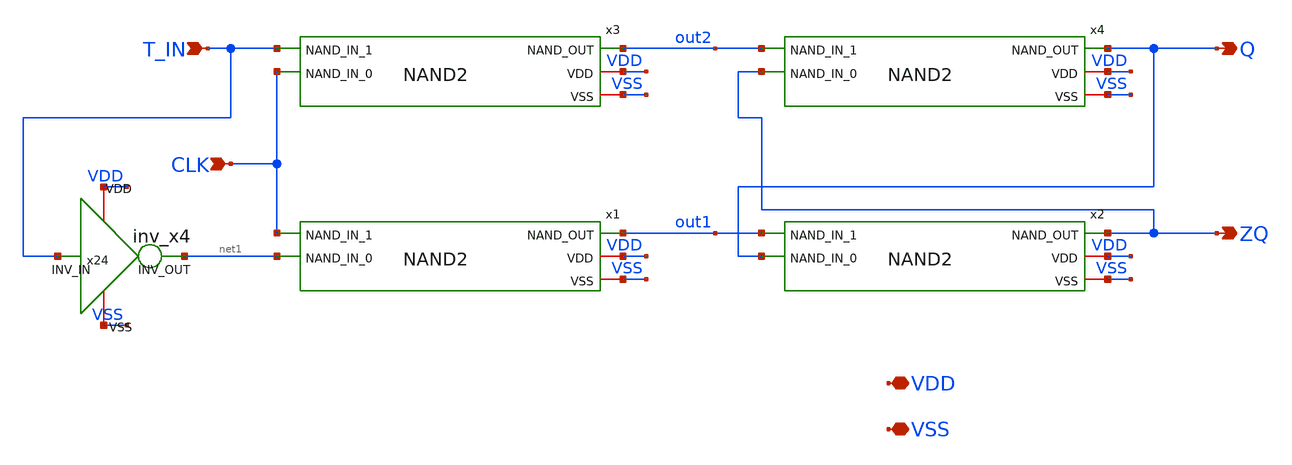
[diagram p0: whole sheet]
** sch_path: xschem/T_FLIP_FLOP.sch
**.subckt T_FLIP_FLOP VDD VSS CLK ZQ Q T_IN
*.iopin VDD
*.iopin VSS
*.ipin CLK
*.opin ZQ
*.opin Q
*.ipin T_IN
x2 ZQ VDD out1 VSS Q NAND2
x4 Q VDD out2 VSS ZQ NAND2
x1 out1 VDD CLK VSS net1 NAND2
x3 out2 VDD T_IN VSS CLK NAND2
x24 VDD VSS net1 T_IN inv_x4
**.ends

* expanding   symbol:  NAND2.sym # of pins=5
** sym_path: xschem/NAND2.sym
** sch_path: xschem/NAND2.sch
.subckt NAND2 NAND_OUT VDD NAND_IN_1 VSS NAND_IN_0
*.ipin NAND_IN_0
*.opin NAND_OUT
*.iopin VDD
*.iopin VSS
*.ipin NAND_IN_1
XM0 net1 NAND_IN_0 VSS VSS sky130_fd_pr__nfet_01v8 L=0.15 W=1 nf=1 ad='int((nf+1)/2) * W/nf * 0.29' as='int((nf+2)/2) * W/nf * 0.29'
+ pd='2*int((nf+1)/2) * (W/nf + 0.29)' ps='2*int((nf+2)/2) * (W/nf + 0.29)' nrd='0.29 / W' nrs='0.29 / W'
+ sa=0 sb=0 sd=0 mult=1 m=1
XM1 NAND_OUT NAND_IN_1 net1 VSS sky130_fd_pr__nfet_01v8 L=0.15 W=1 nf=1 ad='int((nf+1)/2) * W/nf * 0.29'
+ as='int((nf+2)/2) * W/nf * 0.29' pd='2*int((nf+1)/2) * (W/nf + 0.29)' ps='2*int((nf+2)/2) * (W/nf + 0.29)'
+ nrd='0.29 / W' nrs='0.29 / W' sa=0 sb=0 sd=0 mult=1 m=1
XM12 NAND_OUT NAND_IN_0 VDD VDD sky130_fd_pr__pfet_01v8 L=0.15 W=1 nf=1 ad='int((nf+1)/2) * W/nf * 0.29'
+ as='int((nf+2)/2) * W/nf * 0.29' pd='2*int((nf+1)/2) * (W/nf + 0.29)' ps='2*int((nf+2)/2) * (W/nf + 0.29)'
+ nrd='0.29 / W' nrs='0.29 / W' sa=0 sb=0 sd=0 mult=1 m=1
XM13 NAND_OUT NAND_IN_1 VDD VDD sky130_fd_pr__pfet_01v8 L=0.15 W=1 nf=1 ad='int((nf+1)/2) * W/nf * 0.29'
+ as='int((nf+2)/2) * W/nf * 0.29' pd='2*int((nf+1)/2) * (W/nf + 0.29)' ps='2*int((nf+2)/2) * (W/nf + 0.29)'
+ nrd='0.29 / W' nrs='0.29 / W' sa=0 sb=0 sd=0 mult=1 m=1
.ends


* expanding   symbol:  inv_x4.sym # of pins=4
** sym_path: xschem/inv_x4.sym
** sch_path: xschem/inv_x4.sch
.subckt inv_x4 VDD VSS INV_OUT INV_IN
*.ipin INV_IN
*.opin INV_OUT
*.iopin VDD
*.iopin VSS
XM3 INV_OUT INV_IN VDD VDD sky130_fd_pr__pfet_01v8 L=10 W=2 nf=1 ad='int((nf+1)/2) * W/nf * 0.29' as='int((nf+2)/2) * W/nf * 0.29'
+ pd='2*int((nf+1)/2) * (W/nf + 0.29)' ps='2*int((nf+2)/2) * (W/nf + 0.29)' nrd='0.29 / W' nrs='0.29 / W'
+ sa=0 sb=0 sd=0 mult=1 m=1
XM5 INV_OUT INV_IN VSS VSS sky130_fd_pr__nfet_01v8 L=10 W=1 nf=1 ad='int((nf+1)/2) * W/nf * 0.29' as='int((nf+2)/2) * W/nf * 0.29'
+ pd='2*int((nf+1)/2) * (W/nf + 0.29)' ps='2*int((nf+2)/2) * (W/nf + 0.29)' nrd='0.29 / W' nrs='0.29 / W'
+ sa=0 sb=0 sd=0 mult=1 m=1
.ends

.end
